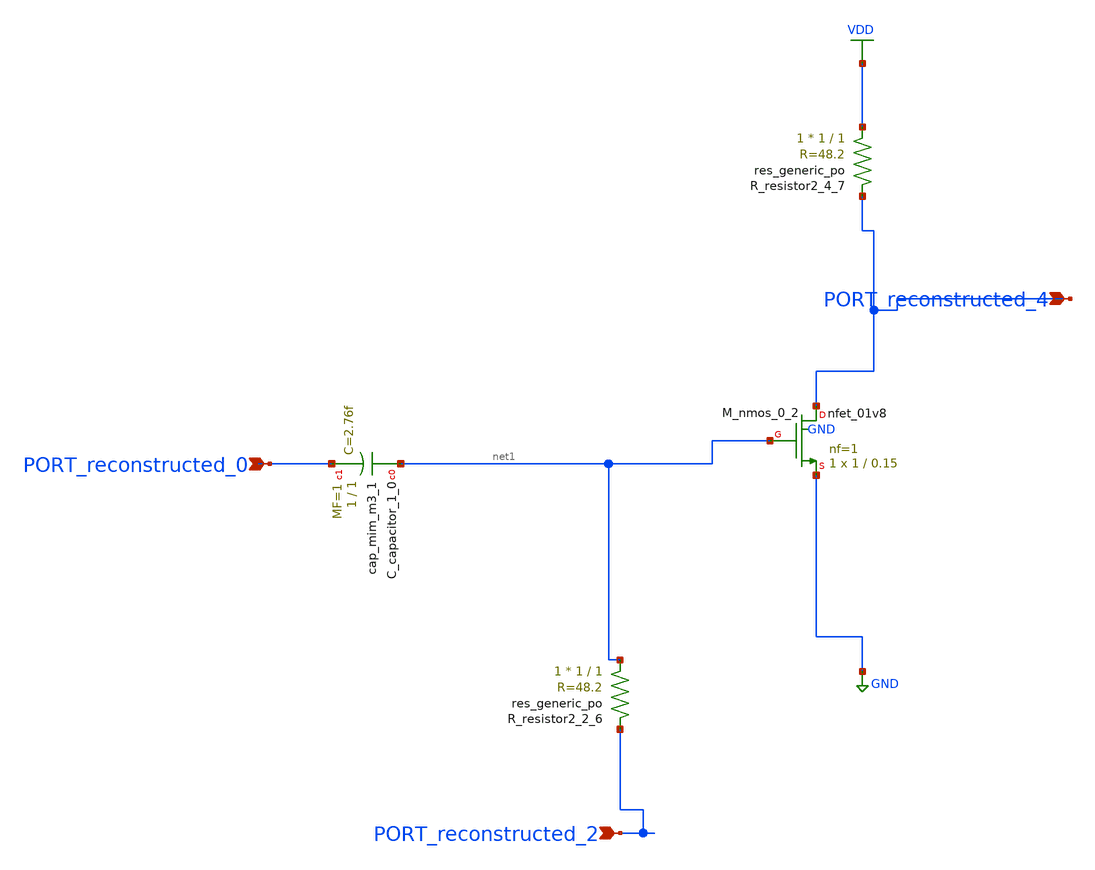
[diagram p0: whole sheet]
** sch_path: schematics/AMSNet/299.sch
**.subckt 299 PORT_reconstructed_2 PORT_reconstructed_4 PORT_reconstructed_0
*.ipin PORT_reconstructed_2
*.ipin PORT_reconstructed_4
*.ipin PORT_reconstructed_0
XC_capacitor_1_0 net1 PORT_reconstructed_0 sky130_fd_pr__cap_mim_m3_1 W=1 L=1 MF=1 m=1
XM_nmos_0_2 PORT_reconstructed_4 net1 GND GND sky130_fd_pr__nfet_01v8 L=0.15 W=1 nf=1 ad='int((1 + 1)/2) * 1 / 1 * 0.29'
+ as='int((1 + 2)/2) * 1 / 1 * 0.29' pd='2*int((1 + 1)/2) * (1 / 1 + 0.29)' ps='2*int((1 + 2)/2) * (1 / 1 + 0.29)'
+ nrd='0.29 / 1 ' nrs='0.29 / 1 ' sa=0 sb=0 sd=0 mult=1 m=1
XR_resistor2_2_6 net1 PORT_reconstructed_2 sky130_fd_pr__res_generic_po W=1 L=1 m=1
XR_resistor2_4_7 VDD PORT_reconstructed_4 sky130_fd_pr__res_generic_po W=1 L=1 m=1
**.ends
.GLOBAL GND
.GLOBAL VDD
.end
